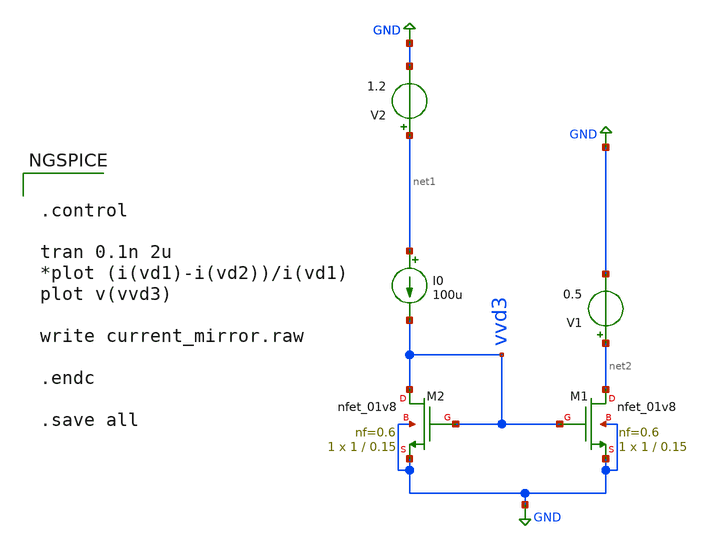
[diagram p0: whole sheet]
** sch_path: current_mirror.sch
**.subckt current_mirror
XM1 net2 vvd3 GND GND sky130_fd_pr__nfet_01v8 L=0.15 W=1 nf=0.6 ad='int((nf+1)/2) * W/nf * 0.29' as='int((nf+2)/2) * W/nf * 0.29'
+ pd='2*int((nf+1)/2) * (W/nf + 0.29)' ps='2*int((nf+2)/2) * (W/nf + 0.29)' nrd='0.29 / W' nrs='0.29 / W'
+ sa=0 sb=0 sd=0 mult=1 m=1
XM2 vvd3 vvd3 GND GND sky130_fd_pr__nfet_01v8 L=0.15 W=1 nf=0.6 ad='int((nf+1)/2) * W/nf * 0.29' as='int((nf+2)/2) * W/nf * 0.29'
+ pd='2*int((nf+1)/2) * (W/nf + 0.29)' ps='2*int((nf+2)/2) * (W/nf + 0.29)' nrd='0.29 / W' nrs='0.29 / W'
+ sa=0 sb=0 sd=0 mult=1 m=1
I0 net1 vvd3 100u
V1 net2 GND 0.5
V2 net1 GND 1.2
**** begin user architecture code


.control

tran 0.1n 2u
*plot (i(vd1)-i(vd2))/i(vd1)
plot v(vvd3)

write current_mirror.raw

.endc

.save all



** opencircuitdesign pdks install
.lib $::SKYWATER_MODELS/sky130.lib.spice tt


**** end user architecture code
**.ends
.GLOBAL GND
.end
